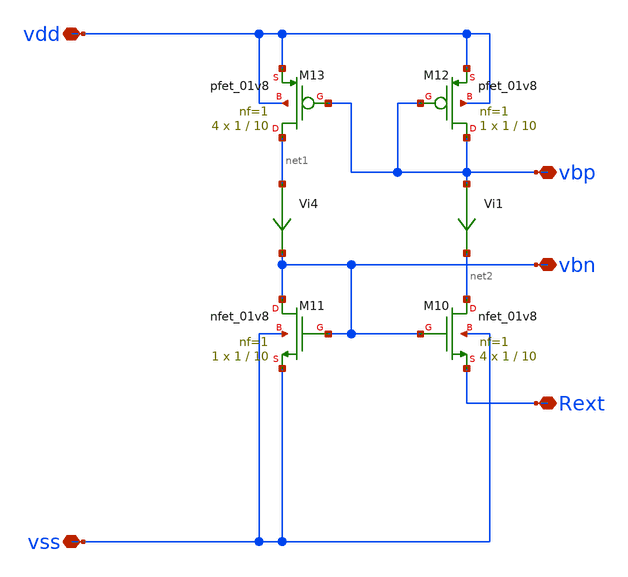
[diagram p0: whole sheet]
** sch_path: playground/ToBias.sch
**.subckt ToBias vss vdd vbp vbn Rext
*.iopin vss
*.iopin vdd
*.iopin vbp
*.iopin vbn
*.iopin Rext
XM10 net2 vbn Rext vss sky130_fd_pr__nfet_01v8 L=10 W=1 nf=1 ad='int((1 + 1)/2) * 1 / 1 * 0.29' as='int((1 + 2)/2) * 1 / 1 * 0.29'
+ pd='2*int((1 + 1)/2) * (1 / 1 + 0.29)' ps='2*int((1 + 2)/2) * (1 / 1 + 0.29)' nrd='0.29 / 1 ' nrs='0.29 / 1 '
+ sa=0 sb=0 sd=0 mult=4 m=4
XM12 vbp vbp vdd vdd sky130_fd_pr__pfet_01v8 L=10 W=1 nf=1 ad='int((nf+1)/2) * W/nf * 0.29' as='int((nf+2)/2) * W/nf * 0.29'
+ pd='2*int((nf+1)/2) * (W/nf + 0.29)' ps='2*int((nf+2)/2) * (W/nf + 0.29)' nrd='0.29 / W' nrs='0.29 / W'
+ sa=0 sb=0 sd=0 mult=1 m=1
XM11 vbn vbn vss vss sky130_fd_pr__nfet_01v8 L=10 W=1 nf=1 ad='int((1 + 1)/2) * 1 / 1 * 0.29' as='int((1 + 2)/2) * 1 / 1 * 0.29'
+ pd='2*int((1 + 1)/2) * (1 / 1 + 0.29)' ps='2*int((1 + 2)/2) * (1 / 1 + 0.29)' nrd='0.29 / 1 ' nrs='0.29 / 1 '
+ sa=0 sb=0 sd=0 mult=1 m=1
XM13 net1 vbp vdd vdd sky130_fd_pr__pfet_01v8 L=10 W=1 nf=1 ad='int((nf+1)/2) * W/nf * 0.29' as='int((nf+2)/2) * W/nf * 0.29'
+ pd='2*int((nf+1)/2) * (W/nf + 0.29)' ps='2*int((nf+2)/2) * (W/nf + 0.29)' nrd='0.29 / W' nrs='0.29 / W'
+ sa=0 sb=0 sd=0 mult=4 m=4
Vi1 vbp net2 0
.save i(vi1)
Vi4 net1 vbn 0
.save i(vi4)
**.ends
.end
